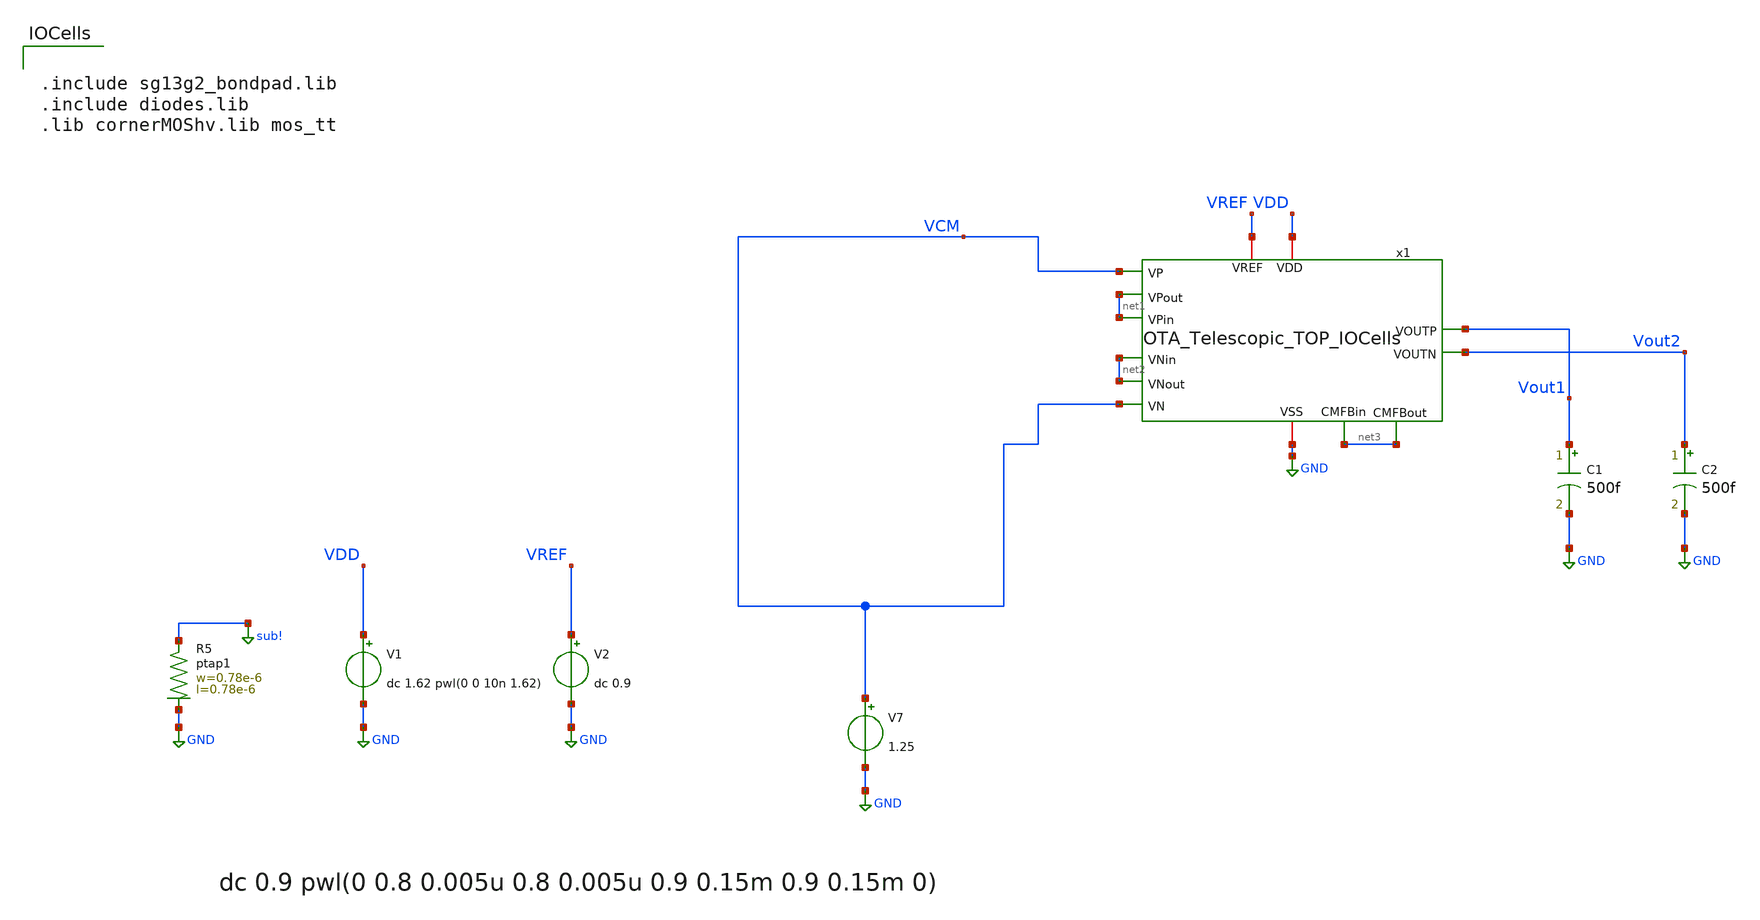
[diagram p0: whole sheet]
** sch_path: OTA_Telescopic/OTA_Telescopic_TOP_TB_StartUp_io.sch
**.subckt OTA_Telescopic_TOP_TB_StartUp_io
V7 VCM GND 1.25
V1 VDD GND dc 1.62 pwl(0 0 10n 1.62)
V2 VREF GND dc 0.9
C1 Vout1 GND 500f m=1
C2 Vout2 GND 500f m=1
XR5 sub! GND ptap1 R=262.8 w=0.78e-6 l=0.78e-6
x1 VDD GND net1 VCM net1 Vout2 Vout1 net2 net2 VCM VREF net3 net3 OTA_Telescopic_TOP_IOCells
**** begin user architecture code

** opencircuitdesign pdks install
.lib cornerMOSlv.lib mos_ss
.lib cornerRES.lib res_typ
.lib cornerCAP.lib cap_typ
.temp 125




.control
 set color0 = white

set wr_singlescale
set wr_vecnames

save all
tran 2.44140625p 1000n
*write NMOS_diode_large_signal.raw

let VCM = v(Vout1)
let VDD = v(VDD)
let IDD = -i(V1)

wrdata VCM_ss_10ns_DC.txt VCM
wrdata IDD_ss_10ns_DC.txt IDD

plot VCM
plot VDD
plot IDD

let Vo1 = v(x1.Vo1)
let Vo2 = v(x1.Vo2)

let Vo = Vo1-Vo2

wrdata Vo Vo

reset
noise v(Vout1) V5 dec 100 1 0.5e9 1
setplot noise1
*plot onoise_spectrum
setplot noise2
print onoise_total

.endc




.include sg13g2_bondpad.lib
.include diodes.lib
.lib cornerMOShv.lib mos_tt


**** end user architecture code
**.ends
.GLOBAL GND
.GLOBAL sub!
.end
